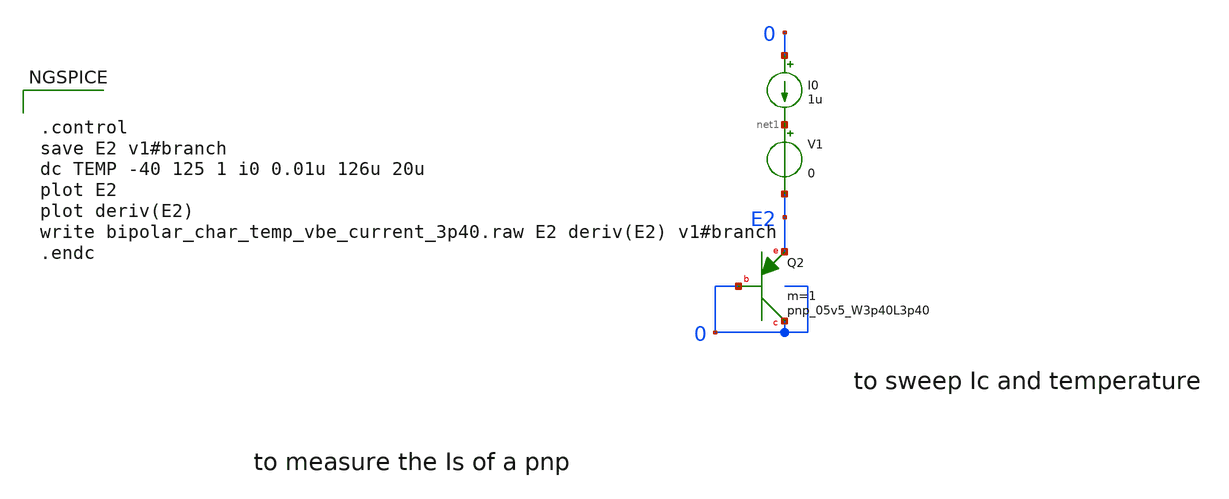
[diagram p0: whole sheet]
** sch_path: schematics/bipolar_characterization_temp_and_vbe_3p40.sch
**.subckt bipolar_characterization_temp_and_vbe_3p40
XQ2 0 0 E2 sky130_fd_pr__pnp_05v5_W3p40L3p40 m=1
I0 0 net1 1u
V1 net1 E2 0
**** begin user architecture code


.control
save E2 v1#branch
dc TEMP -40 125 1 i0 0.01u 126u 20u
plot E2
plot deriv(E2)
write bipolar_char_temp_vbe_current_3p40.raw E2 deriv(E2) v1#branch
.endc


 .lib $SKYWATER_MODELS/sky130.lib.spice tt
.include $SKYWATER_CELLS/pnp_05v5/sky130_fd_pr__pnp_05v5_W3p40L3p40.model.spice

**** end user architecture code
**.ends
.end
